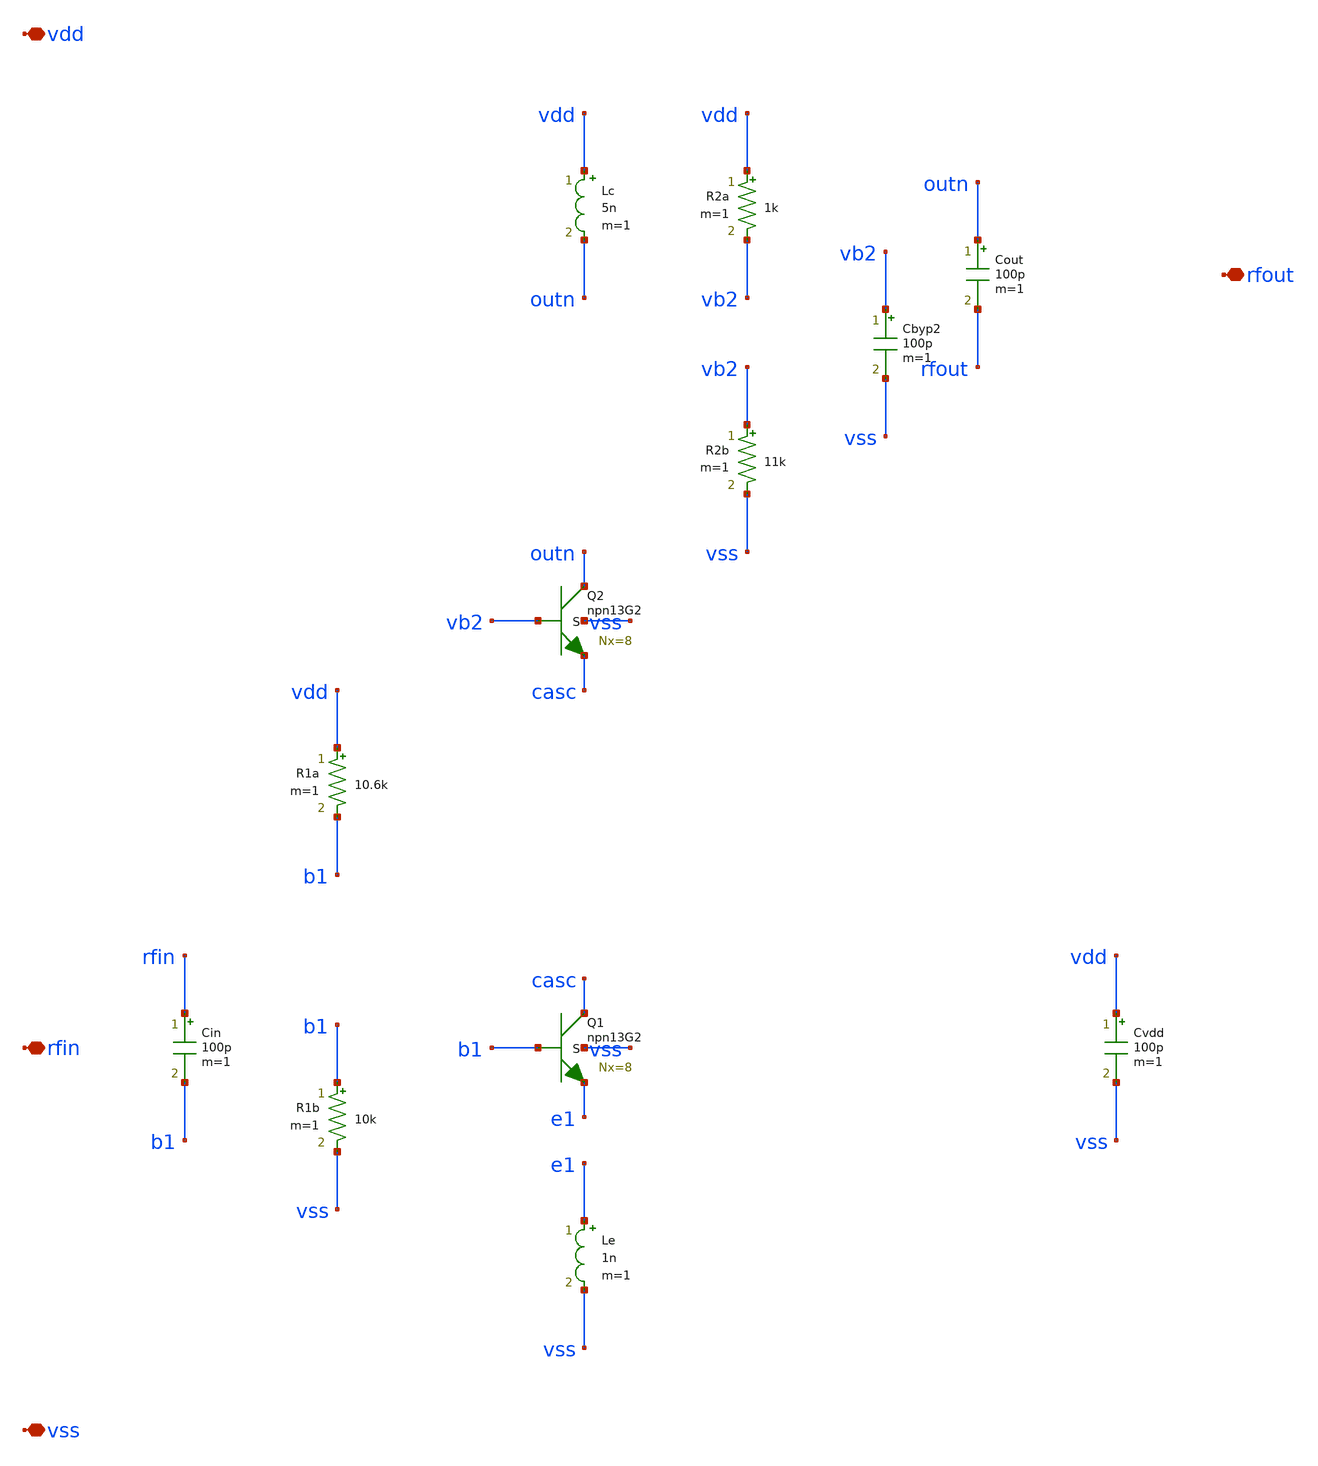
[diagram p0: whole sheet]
** sch_path: design/lna.sch
**.subckt lna vdd vss rfin rfout
*.iopin vdd
*.iopin vss
*.iopin rfin
*.iopin rfout
XQ2 outn vb2 casc vss npn13G2 Nx=8 mm_ok=1
XQ1 casc b1 e1 vss npn13G2 Nx=8 mm_ok=1
Le e1 vss 1n m=1
Lc vdd outn 5n m=1
Cin rfin b1 100p m=1
Cout outn rfout 100p m=1
Cbyp2 vb2 vss 100p m=1
Cvdd vdd vss 100p m=1
R2a vdd vb2 1k m=1
R2b vb2 vss 11k m=1
R1a vdd b1 10.6k m=1
R1b b1 vss 10k m=1
**.ends
.end
